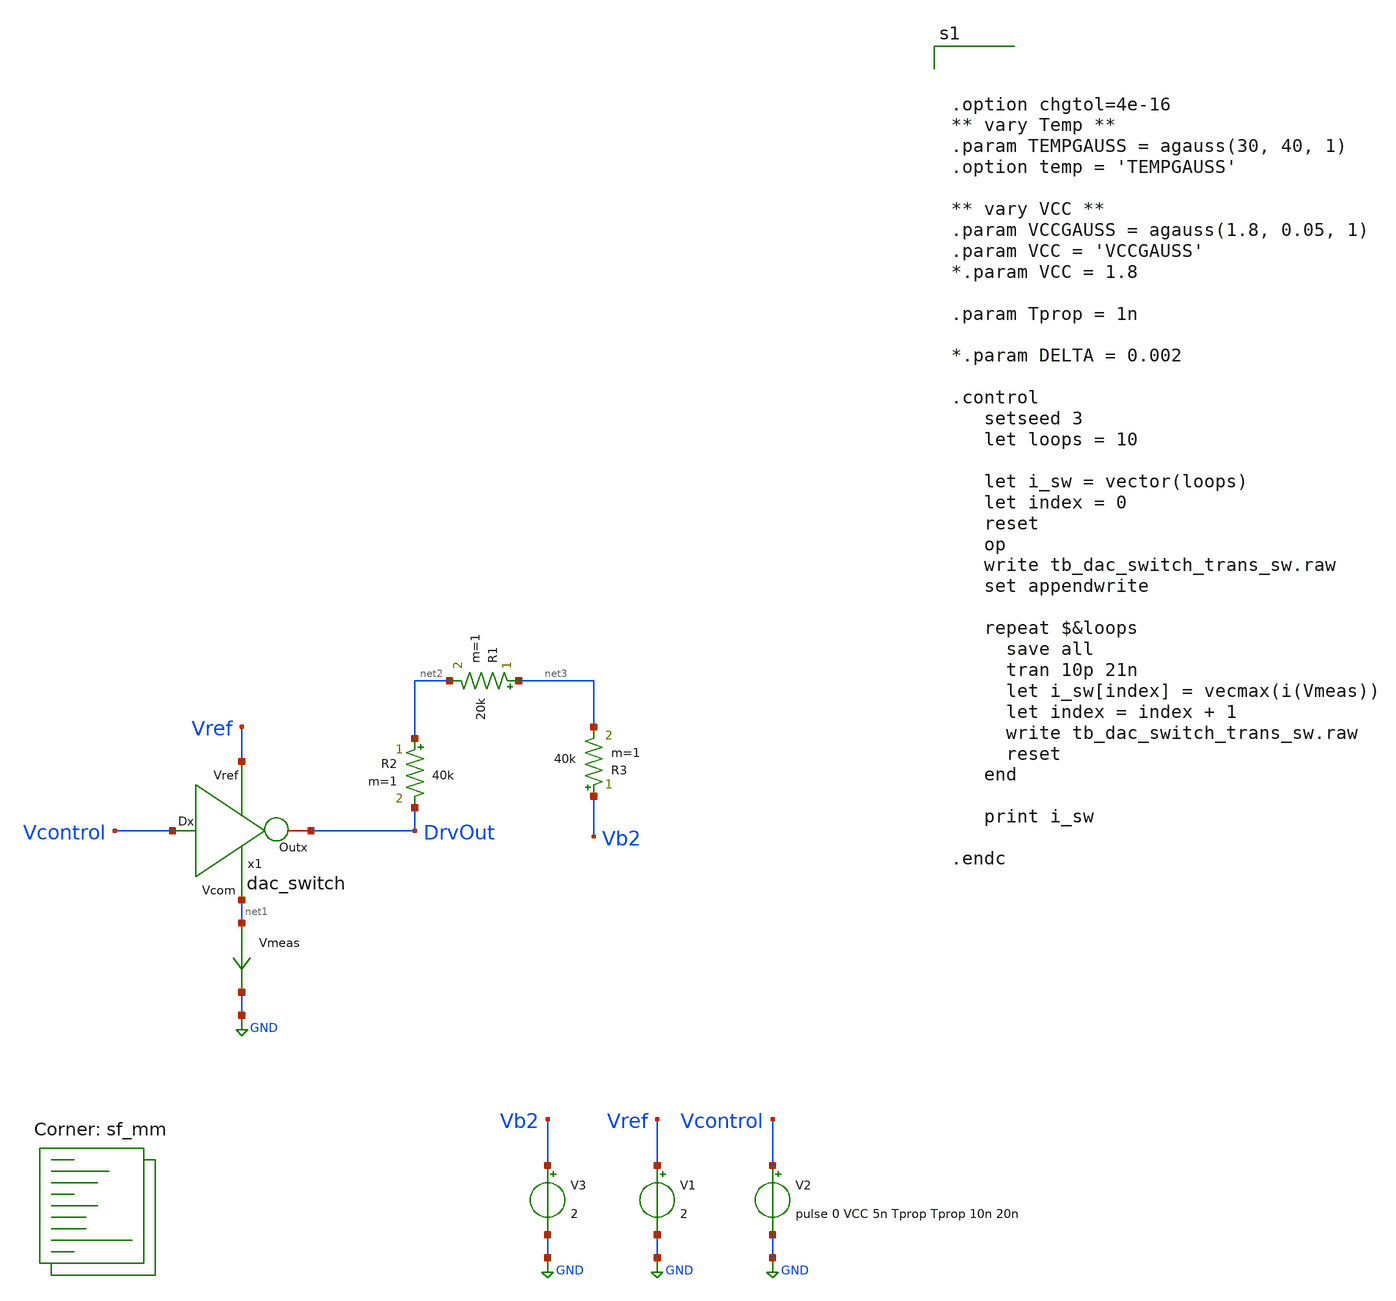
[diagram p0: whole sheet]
** sch_path: xschem/tb_dac_switch_trans_sw.sch
**.subckt tb_dac_switch_trans_sw
V1 Vref GND 2
x1 Vref Vcontrol DrvOut net1 dac_switch
V2 Vcontrol GND pulse 0 VCC 5n Tprop Tprop 10n 20n
R2 net2 DrvOut 40k m=1
R1 net3 net2 20k m=1
R3 Vb2 net3 40k m=1
V3 Vb2 GND 2
Vmeas net1 GND 0
.save i(vmeas)
**** begin user architecture code
.lib $::SKYWATER_MODELS/sky130.lib.spice sf_mm



.option chgtol=4e-16
** vary Temp **
.param TEMPGAUSS = agauss(30, 40, 1)
.option temp = 'TEMPGAUSS'

** vary VCC **
.param VCCGAUSS = agauss(1.8, 0.05, 1)
.param VCC = 'VCCGAUSS'
*.param VCC = 1.8

.param Tprop = 1n

*.param DELTA = 0.002

.control
   setseed 3
   let loops = 10

   let i_sw = vector(loops)
   let index = 0
   reset
   op
   write tb_dac_switch_trans_sw.raw
   set appendwrite

   repeat $&loops
     save all
     tran 10p 21n
     let i_sw[index] = vecmax(i(Vmeas))
     let index = index + 1
     write tb_dac_switch_trans_sw.raw
     reset
   end

   print i_sw

.endc



**** end user architecture code
**.ends

* expanding   symbol:  dac_switch.sym # of pins=4
** sym_path: xschem/dac_switch.sym
** sch_path: xschem/dac_switch.sch
.subckt dac_switch Vref Dx Outx Vcom
*.ipin Dx
*.opin Outx
*.iopin Vref
*.iopin Vcom
XM1 Outx Dx Vref Vref sky130_fd_pr__pfet_g5v0d10v5 L=0.5 W=16 nf=1 ad='int((nf+1)/2) * W/nf * 0.29' as='int((nf+2)/2) * W/nf * 0.29'
+ pd='2*int((nf+1)/2) * (W/nf + 0.29)' ps='2*int((nf+2)/2) * (W/nf + 0.29)' nrd='0.29 / W' nrs='0.29 / W'
+ sa=0 sb=0 sd=0 mult=1 m=1
XM2 Outx Dx Vcom Vcom sky130_fd_pr__nfet_g5v0d10v5 L=0.5 W=7 nf=1 ad='int((nf+1)/2) * W/nf * 0.29' as='int((nf+2)/2) * W/nf * 0.29'
+ pd='2*int((nf+1)/2) * (W/nf + 0.29)' ps='2*int((nf+2)/2) * (W/nf + 0.29)' nrd='0.29 / W' nrs='0.29 / W'
+ sa=0 sb=0 sd=0 mult=1 m=1
.ends

.GLOBAL GND
.end
